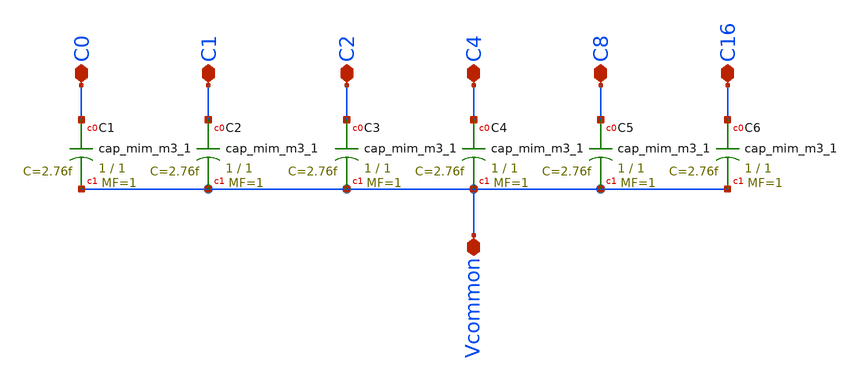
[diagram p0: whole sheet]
** sch_path: untitled.sch
**.subckt untitled C0 C1 C2 C4 C8 C16 Vcommon
*.iopin C0
*.iopin C1
*.iopin C2
*.iopin C4
*.iopin C8
*.iopin C16
*.iopin Vcommon
XC1 C0 Vcommon sky130_fd_pr__cap_mim_m3_1 W=1 L=1 MF=1 m=1
XC2 C1 Vcommon sky130_fd_pr__cap_mim_m3_1 W=1 L=1 MF=1 m=1
XC3 C2 Vcommon sky130_fd_pr__cap_mim_m3_1 W=1 L=1 MF=1 m=1
XC4 C4 Vcommon sky130_fd_pr__cap_mim_m3_1 W=1 L=1 MF=1 m=1
XC5 C8 Vcommon sky130_fd_pr__cap_mim_m3_1 W=1 L=1 MF=1 m=1
XC6 C16 Vcommon sky130_fd_pr__cap_mim_m3_1 W=1 L=1 MF=1 m=1
**.ends
.end
